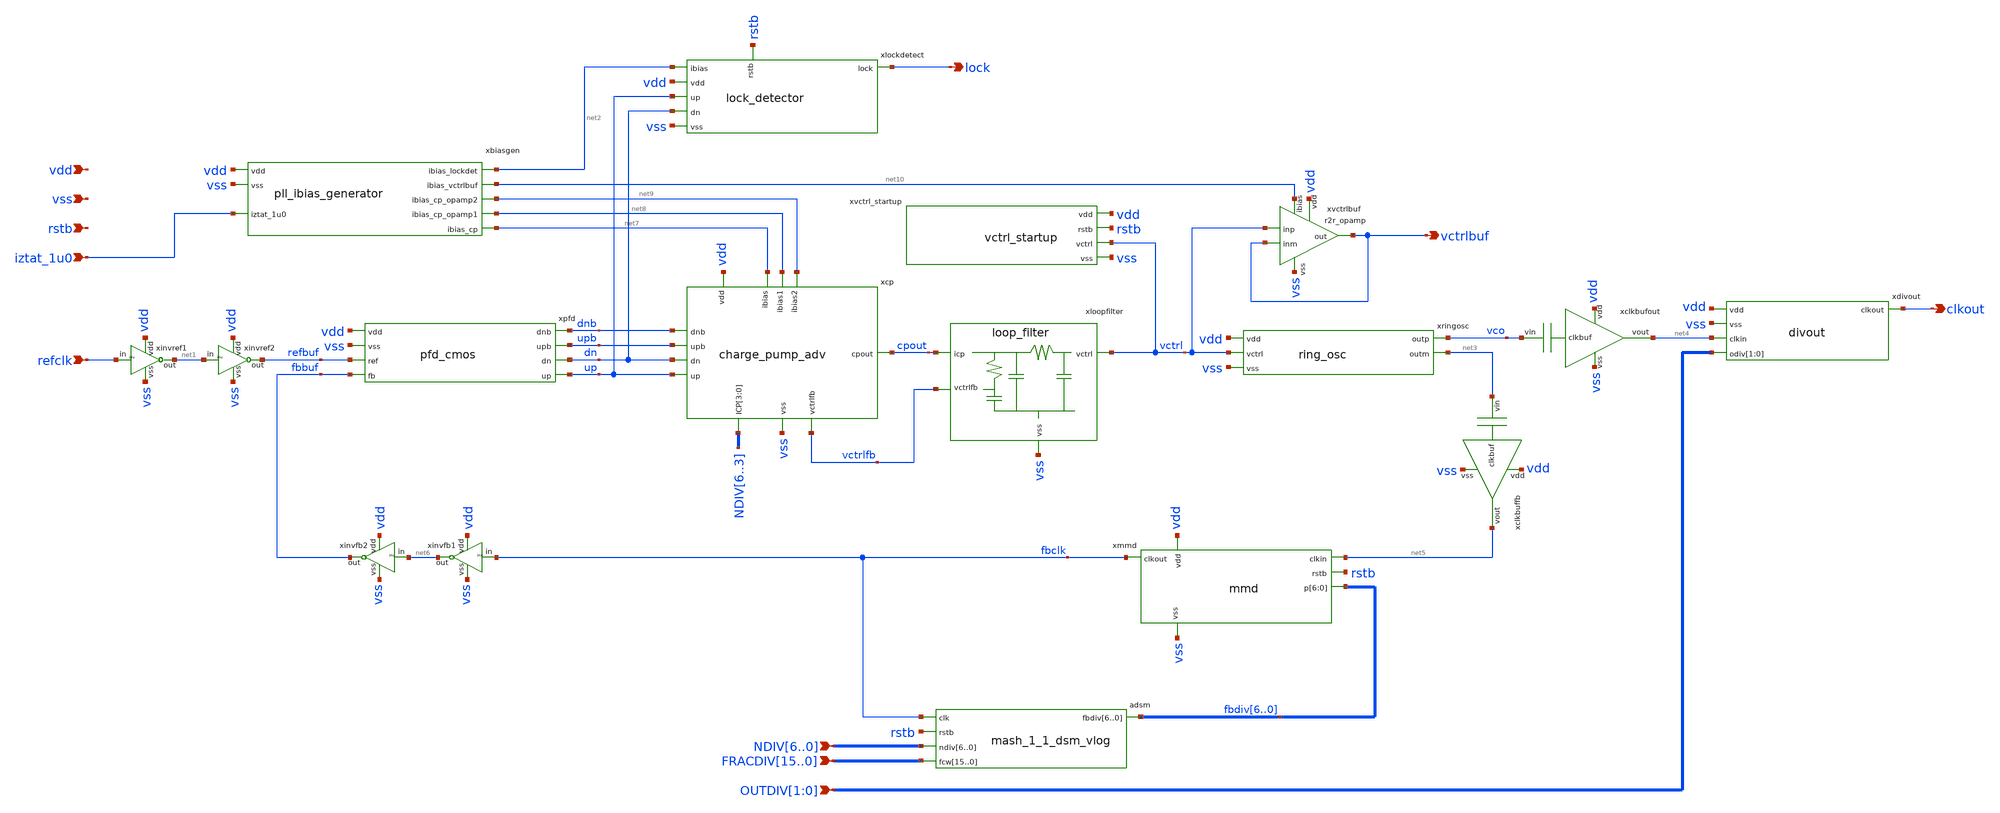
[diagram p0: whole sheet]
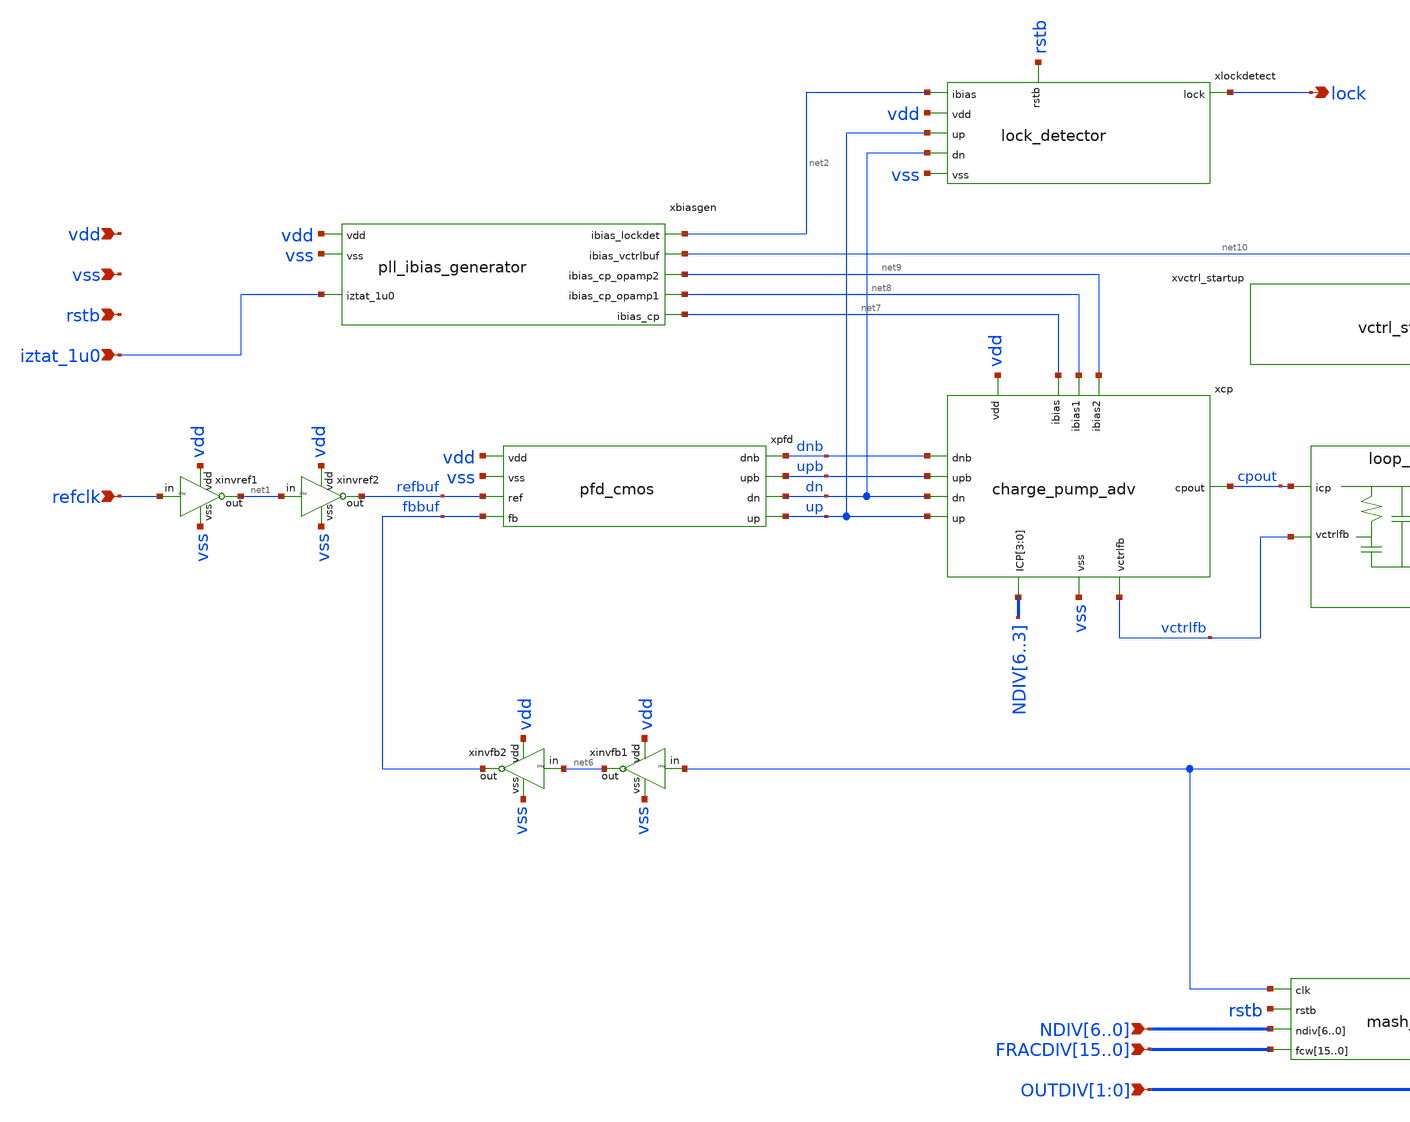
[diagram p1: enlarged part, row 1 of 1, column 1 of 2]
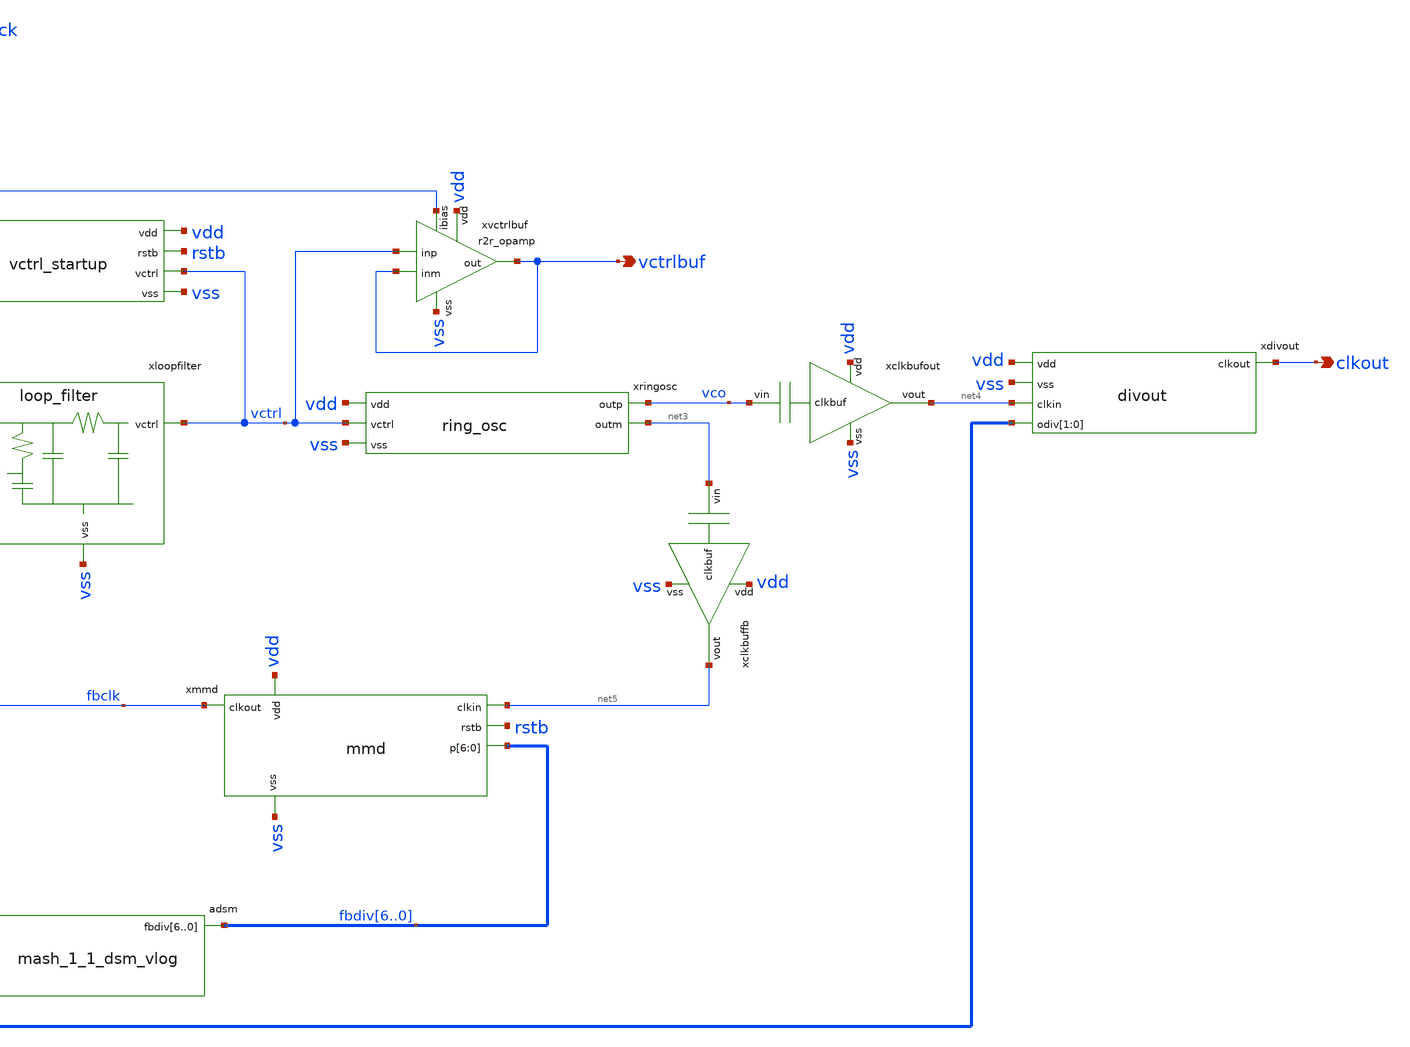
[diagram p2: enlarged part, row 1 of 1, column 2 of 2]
** sch_path: xschem/gf180mcu_tjd_ip_rofncppll__vlog_dsm.sch
**.subckt gf180mcu_tjd_ip_rofncppll__vlog_dsm refclk lock vctrlbuf vdd vss clkout
*+ NDIV6,NDIV5,NDIV4,NDIV3,NDIV2,NDIV1,NDIV0
*+ FRACDIV15,FRACDIV14,FRACDIV13,FRACDIV12,FRACDIV11,FRACDIV10,FRACDIV9,FRACDIV8,FRACDIV7,FRACDIV6,FRACDIV5,FRACDIV4,FRACDIV3,FRACDIV2,FRACDIV1,FRACDIV0 OUTDIV[1],OUTDIV[0] iztat_1u0 rstb
*.ipin refclk
*.opin lock
*.opin vctrlbuf
*.ipin vdd
*.ipin vss
*.opin clkout
*.ipin NDIV6,NDIV5,NDIV4,NDIV3,NDIV2,NDIV1,NDIV0
*.ipin
*+ FRACDIV15,FRACDIV14,FRACDIV13,FRACDIV12,FRACDIV11,FRACDIV10,FRACDIV9,FRACDIV8,FRACDIV7,FRACDIV6,FRACDIV5,FRACDIV4,FRACDIV3,FRACDIV2,FRACDIV1,FRACDIV0
*.ipin OUTDIV[1],OUTDIV[0]
*.ipin iztat_1u0
*.ipin rstb
xinvref1 vdd refclk net1 vss inv
xinvref2 vdd net1 refbuf vss inv
xpfd vdd vss dnb upb refbuf fbbuf dn up pfd_cmos
xcp vdd up upb net8 net9 cpout net7 dnb dn vss vctrlfb NDIV6 NDIV5 NDIV4 NDIV3 charge_pump_adv
xlockdetect net2 vdd up dn lock vss rstb lock_detector
xringosc vco net3 vdd vctrl vss ring_osc
xdivout vdd vss clkout net4 OUTDIV[1] OUTDIV[0] divout
xclkbuffb vdd net3 net5 vss clkbuf
xclkbufout vdd vco net4 vss clkbuf
xmmd fbclk net5 vdd vss rstb fbdiv6 fbdiv5 fbdiv4 fbdiv3 fbdiv2 fbdiv1 fbdiv0 mmd
xloopfilter cpout vctrl vctrlfb vss loop_filter
xvctrlbuf vdd vctrlbuf net10 vctrl vctrlbuf vss r2r_opamp
xinvfb1 vdd fbclk net6 vss inv
xinvfb2 vdd net6 fbbuf vss inv
xbiasgen vdd iztat_1u0 net2 net10 net9 net8 net7 vss pll_ibias_generator
xvctrl_startup vdd rstb vctrl vss vctrl_startup
adsm [ fbclk rstb NDIV6 NDIV5 NDIV4 NDIV3 NDIV2 NDIV1 NDIV0 FRACDIV15 FRACDIV14 FRACDIV13 FRACDIV12
+ FRACDIV11 FRACDIV10 FRACDIV9 FRACDIV8 FRACDIV7 FRACDIV6 FRACDIV5 FRACDIV4 FRACDIV3 FRACDIV2 FRACDIV1 FRACDIV0
+ ] [ fbdiv6 fbdiv5 fbdiv4 fbdiv3 fbdiv2 fbdiv1 fbdiv0 ] dut
**.ends
**** begin user architecture code
.model dut d_cosim simulation="ivlng" sim_args=["mash_1_1_dsm"]
**** end user architecture code
.end
